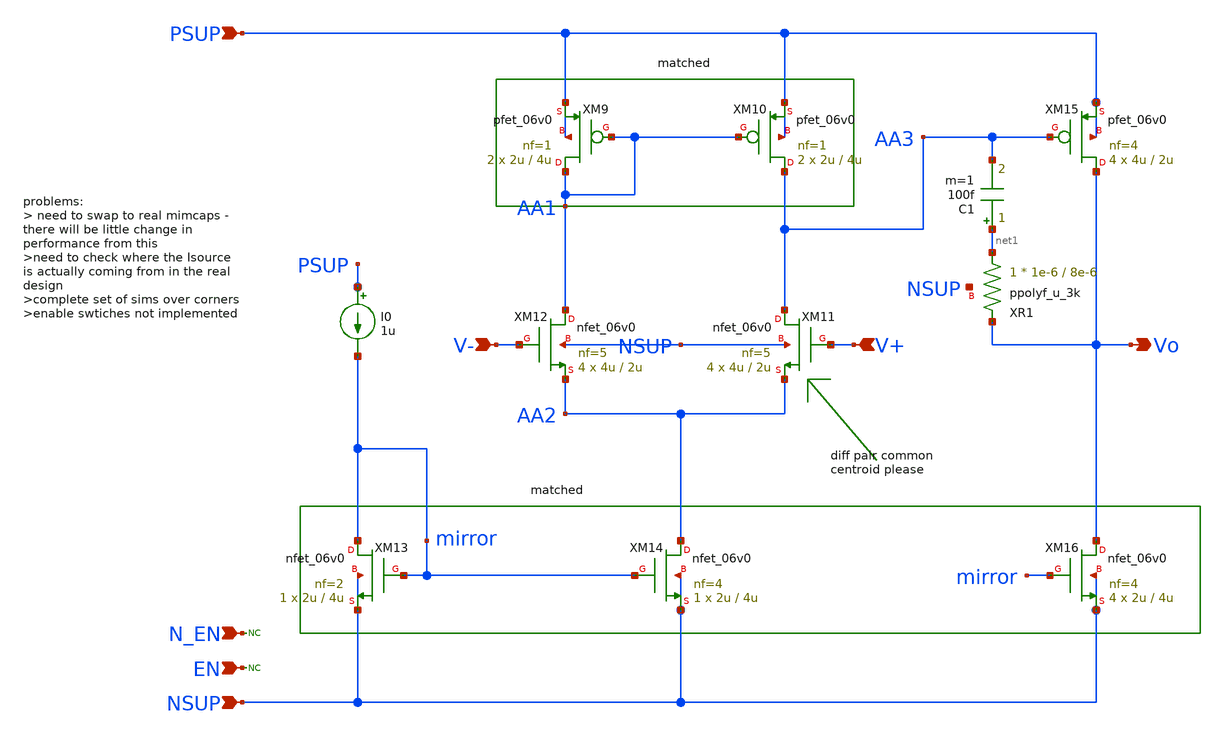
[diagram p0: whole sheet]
** sch_path: xschem/blocks/aux_buff/aux_amp.sch
**.subckt aux_amp PSUP NSUP N_EN EN Vo V+ V-
*.ipin PSUP
*.ipin NSUP
*.ipin N_EN
*.ipin EN
*.opin Vo
*.ipin V+
*.ipin V-
XM9 AA1 AA1 PSUP PSUP pfet_06v0 L=4u W=2u nf=1 ad='int((nf+1)/2) * W/nf * 0.18u' as='int((nf+2)/2) * W/nf * 0.18u'
+ pd='2*int((nf+1)/2) * (W/nf + 0.18u)' ps='2*int((nf+2)/2) * (W/nf + 0.18u)' nrd='0.18u / W' nrs='0.18u / W'
+ sa=0 sb=0 sd=0 m=2
XM10 AA3 AA1 PSUP PSUP pfet_06v0 L=4u W=2u nf=1 ad='int((nf+1)/2) * W/nf * 0.18u' as='int((nf+2)/2) * W/nf * 0.18u'
+ pd='2*int((nf+1)/2) * (W/nf + 0.18u)' ps='2*int((nf+2)/2) * (W/nf + 0.18u)' nrd='0.18u / W' nrs='0.18u / W'
+ sa=0 sb=0 sd=0 m=2
* noconn N_EN
* noconn EN
XM11 AA3 V+ AA2 NSUP nfet_06v0 L=2u W=4u nf=5 ad='int((nf+1)/2) * W/nf * 0.18u' as='int((nf+2)/2) * W/nf * 0.18u'
+ pd='2*int((nf+1)/2) * (W/nf + 0.18u)' ps='2*int((nf+2)/2) * (W/nf + 0.18u)' nrd='0.18u / W' nrs='0.18u / W'
+ sa=0 sb=0 sd=0 m=4
XM12 AA1 V- AA2 NSUP nfet_06v0 L=2u W=4u nf=5 ad='int((nf+1)/2) * W/nf * 0.18u' as='int((nf+2)/2) * W/nf * 0.18u'
+ pd='2*int((nf+1)/2) * (W/nf + 0.18u)' ps='2*int((nf+2)/2) * (W/nf + 0.18u)' nrd='0.18u / W' nrs='0.18u / W'
+ sa=0 sb=0 sd=0 m=4
C1 net1 AA3 100f m=1
XM13 mirror mirror NSUP NSUP nfet_06v0 L=4u W=2u nf=2 ad='int((nf+1)/2) * W/nf * 0.18u' as='int((nf+2)/2) * W/nf * 0.18u'
+ pd='2*int((nf+1)/2) * (W/nf + 0.18u)' ps='2*int((nf+2)/2) * (W/nf + 0.18u)' nrd='0.18u / W' nrs='0.18u / W'
+ sa=0 sb=0 sd=0 m=1
I0 PSUP mirror 1u
XM14 AA2 mirror NSUP NSUP nfet_06v0 L=4u W=2u nf=4 ad='int((nf+1)/2) * W/nf * 0.18u' as='int((nf+2)/2) * W/nf * 0.18u'
+ pd='2*int((nf+1)/2) * (W/nf + 0.18u)' ps='2*int((nf+2)/2) * (W/nf + 0.18u)' nrd='0.18u / W' nrs='0.18u / W'
+ sa=0 sb=0 sd=0 m=1
XM15 Vo AA3 PSUP PSUP pfet_06v0 L=2u W=4u nf=4 ad='int((nf+1)/2) * W/nf * 0.18u' as='int((nf+2)/2) * W/nf * 0.18u'
+ pd='2*int((nf+1)/2) * (W/nf + 0.18u)' ps='2*int((nf+2)/2) * (W/nf + 0.18u)' nrd='0.18u / W' nrs='0.18u / W'
+ sa=0 sb=0 sd=0 m=4
XM16 Vo mirror NSUP NSUP nfet_06v0 L=4u W=2u nf=4 ad='int((nf+1)/2) * W/nf * 0.18u' as='int((nf+2)/2) * W/nf * 0.18u'
+ pd='2*int((nf+1)/2) * (W/nf + 0.18u)' ps='2*int((nf+2)/2) * (W/nf + 0.18u)' nrd='0.18u / W' nrs='0.18u / W'
+ sa=0 sb=0 sd=0 m=4
XR1 net1 Vo NSUP ppolyf_u_3k r_width=1e-6 r_length=8e-6 m=1
**.ends
.end
